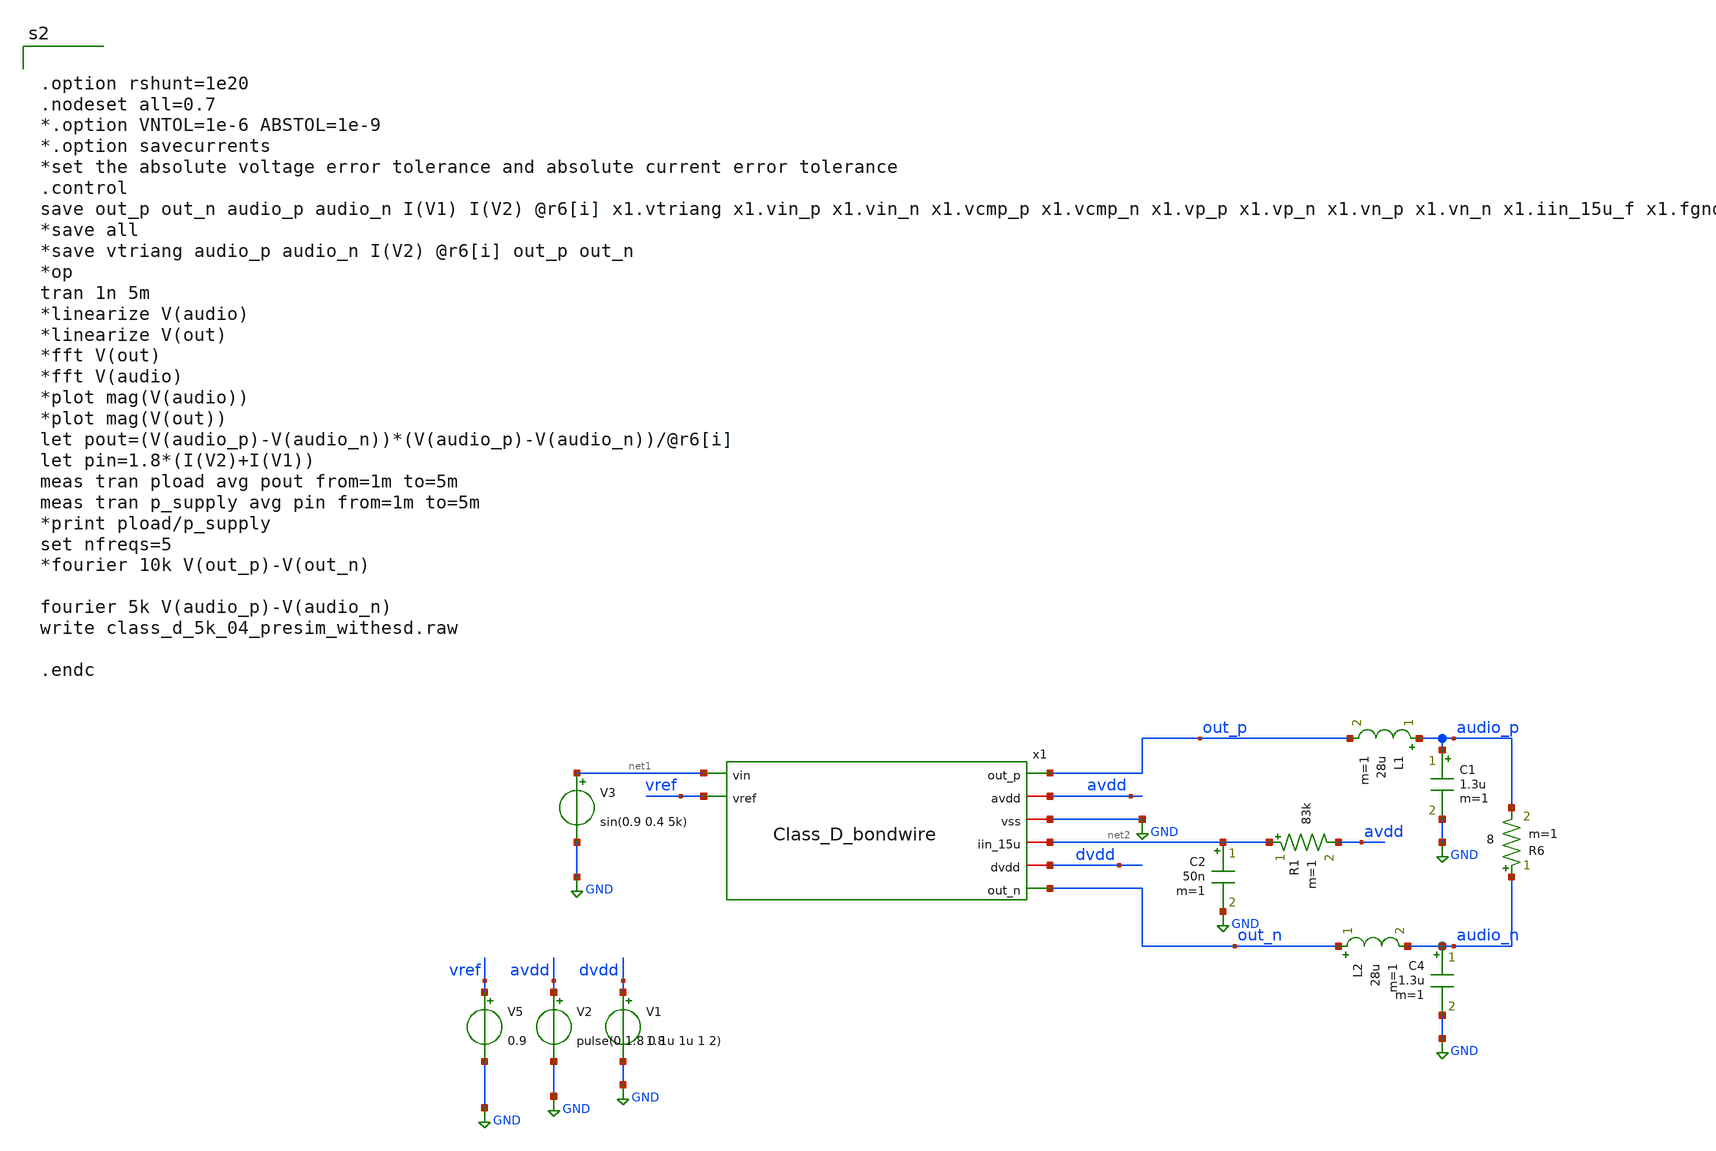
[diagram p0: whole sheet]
** sch_path: xschem/src/Class_D/Class_D_tb2.sch
**.subckt Class_D_tb2
V5 vref GND 0.9
V1 dvdd GND 1.8
V2 avdd GND pulse(0 1.8 0 1u 1u 1 2)
V3 net1 GND sin(0.9 0.4 5k)
L1 audio_p out_p 28u m=1
C1 audio_p GND 1.3u m=1
L2 out_n audio_n 28u m=1
C4 audio_n GND 1.3u m=1
R6 audio_n audio_p 8 m=1
x1 out_p net1 avdd vref GND net2 dvdd out_n Class_D_bondwire
R1 net2 avdd 83k m=1
C2 net2 GND 50n m=1
**** begin user architecture code

.include /home/eda/pdk/skywater-pdk/libraries/sky130_fd_pr_ngspice/latest/models/corners/tt.spice
.include /home/eda/magic/class_d_audio_amplifier/Class_D/Class_D_post.spice

* Resistor$::SKYWATER_MODELS/Capacitor
.include $::SKYWATER_MODELS/models/r+c/res_typical__cap_typical.spice
.include $::SKYWATER_MODELS/models/r+c/res_typical__cap_typical__lin.spice
* Special cells
.include $::SKYWATER_MODELS/models/corners/tt/specialized_cells.spice




.option rshunt=1e20
.nodeset all=0.7
*.option VNTOL=1e-6 ABSTOL=1e-9
*.option savecurrents
*set the absolute voltage error tolerance and absolute current error tolerance
.control
save out_p out_n audio_p audio_n I(V1) I(V2) @r6[i] x1.vtriang x1.vin_p x1.vin_n x1.vcmp_p x1.vcmp_n
+ x1.vp_p x1.vp_n x1.vn_p x1.vn_n x1.iin_15u_f x1.fgnd
*save all
*save vtriang audio_p audio_n I(V2) @r6[i] out_p out_n
*op
tran 1n 5m
*linearize V(audio)
*linearize V(out)
*fft V(out)
*fft V(audio)
*plot mag(V(audio))
*plot mag(V(out))
let pout=(V(audio_p)-V(audio_n))*(V(audio_p)-V(audio_n))/@r6[i]
let pin=1.8*(I(V2)+I(V1))
meas tran pload avg pout from=1m to=5m
meas tran p_supply avg pin from=1m to=5m
*print pload/p_supply
set nfreqs=5
*fourier 10k V(out_p)-V(out_n)

fourier 5k V(audio_p)-V(audio_n)
write class_d_5k_04_presim_withesd.raw

.endc




**** end user architecture code
**.ends

* expanding   symbol:  src/Class_D/Class_D_bondwire.sym # of pins=8
** sym_path: xschem/src/Class_D/Class_D_bondwire.sym
** sch_path: xschem/src/Class_D/Class_D_bondwire.sch
.subckt Class_D_bondwire out_p vin avdd vref vss iin_15u dvdd out_n
*.opin out_p
*.opin out_n
*.ipin vin
*.ipin vref
*.iopin avdd
*.iopin vss
*.iopin iin_15u
*.iopin dvdd
x1 vp_p out_p_f vp_n vin_p vcmp_p vtriang vin_f avdd_f vin_n fgnd vcmp_n iin_15u_f vn_p dvdd_f vn_n
+ out_n_f net8 Class_D
R1 net1 out_p_f 0.2m m=1
L1 out_p net1 0.011n m=1
C1 out_p vss 0.06p m=1
C2 out_p_f vss 0.06p m=1
R2 net2 avdd_f 0.3m m=1
L2 avdd net2 0.016n m=1
C3 avdd vss 0.04p m=1
C4 avdd_f vss 0.04p m=1
R3 net3 iin_15u_f 0.6m m=1
L3 iin_15u net3 0.032n m=1
C5 iin_15u vss 0.02p m=1
C6 iin_15u_f vss 0.02p m=1
R4 net4 dvdd_f 0.2m m=1
L4 dvdd net4 0.011n m=1
C7 dvdd vss 0.06p m=1
C8 dvdd_f vss 0.06p m=1
R5 net5 out_n_f 0.2m m=1
L5 out_n net5 0.011n m=1
C9 out_n vss 0.06p m=1
C10 out_n_f vss 0.06p m=1
R6 net6 vin_f 0.6m m=1
L6 vin net6 0.032n m=1
C11 vin vss 0.02p m=1
C12 vin_f vss 0.02p m=1
R7 net7 net8 0.6m m=1
L7 vref net7 0.032n m=1
C13 vref vss 0.02p m=1
C14 net8 vss 0.02p m=1
R8 net9 fgnd 0.15m m=1
L8 vss net9 0.008n m=1
C15 vss vss 0.08p m=1
C16 fgnd vss 0.08p m=1
x2 dvdd_f out_p_f fgnd ESD
x3 avdd_f iin_15u_f fgnd ESD
x4 dvdd_f out_n_f fgnd ESD
x5 avdd_f vin_f fgnd ESD
x6 avdd_f net8 fgnd ESD
x7 avdd_f fgnd io_clamp
x8 dvdd_f fgnd io_clamp
.ends


* expanding   symbol:  src/Class_D/Class_D.sym # of pins=17
** sym_path: xschem/src/Class_D/Class_D.sym
** sch_path: xschem/src/Class_D/Class_D.sch
.subckt Class_D vp_p out_p vp_n vin_p vcmp_p vtriang vin avdd vin_n vss vcmp_n iin_15u vn_p dvdd
+ vn_n out_n vref
*.ipin vin
*.iopin avdd
*.opin out_n
*.iopin vss
*.iopin iin_15u
*.opin out_p
*.opin vtriang
*.iopin dvdd
*.opin vin_p
*.opin vin_n
*.opin vcmp_p
*.opin vcmp_n
*.opin vp_p
*.opin vp_n
*.opin vn_p
*.opin vn_n
*.ipin vref
x1 avdd vbias3 vbias6 vin vref vss vin_n vin_p S_to_D
x2 avdd vbias5 vbias4 vref vss vsquare vtriang triangle
x3 avdd feedback_p vbias2 vref vss error_p integrator
x4 avdd feedback_n vbias7 vref vss error_n integrator
x5 avdd error_p vtriang vbias1 vss vcmp_p comparator
x6 avdd error_n vtriang vbias8 vss vcmp_n comparator
x7 dvdd vcmp_p vp_p vp_n vss dead_time
x8 dvdd vcmp_n vn_p vn_n vss dead_time
x10 iin_15u vbias1 vbias2 vbias3 vbias4 vbias5 vbias6 vbias7 vbias8 vss biasing_network
XR1 feedback_p vin_p vss sky130_fd_pr__res_xhigh_po W=0.35 L=35 mult=1 m=1
XR2 vin_n feedback_n vss sky130_fd_pr__res_xhigh_po W=0.35 L=35 mult=1 m=1
x9 dvdd vp_p out_p vss vp_n dvdd vn_p out_n vn_n output_driver
XC1 vss dvdd sky130_fd_pr__cap_mim_m3_2 W=16 L=16 MF=90 m=90
XC2 dvdd vss sky130_fd_pr__cap_mim_m3_2 W=30 L=30 MF=262 m=262
XC3 avdd vss sky130_fd_pr__cap_mim_m3_2 W=30 L=30 MF=132 m=132
XC4 avdd vss sky130_fd_pr__cap_mim_m3_2 W=30 L=30 MF=132 m=132
XR3 out_p feedback_p vss sky130_fd_pr__res_xhigh_po W=0.35 L=35 mult=1 m=1
XR4 out_n feedback_n vss sky130_fd_pr__res_xhigh_po W=0.35 L=35 mult=1 m=1
XC5 iin_15u vss sky130_fd_pr__cap_mim_m3_2 W=30 L=30 MF=210 m=210
.ends


* expanding   symbol:  src/ESD/ESD.sym # of pins=3
** sym_path: xschem/src/ESD/ESD.sym
** sch_path: xschem/src/ESD/ESD.sch
.subckt ESD vdd vin vss
*.iopin vdd
*.iopin vin
*.iopin vss
XD17 vin vdd sky130_fd_pr__diode_pd2nw_05v5 area=22500 pj=4e6
XD1 vss vin sky130_fd_pr__diode_pw2nd_05v5 area=22500 pj=4e6
.ends


* expanding   symbol:  src/ESD/io_clamp.sym # of pins=2
** sym_path: xschem/src/ESD/io_clamp.sym
** sch_path: xschem/src/ESD/io_clamp.sch
.subckt io_clamp vdd vss
*.iopin vdd
*.iopin vss
XD4 net3 net2 sky130_fd_pr__diode_pd2nw_05v5 area=22500 pj=4e6
XD1 net1 net3 sky130_fd_pr__diode_pd2nw_05v5 area=22500 pj=4e6
XD2 vdd net1 sky130_fd_pr__diode_pd2nw_05v5 area=22500 pj=4e6
XD3 net2 vss sky130_fd_pr__diode_pd2nw_05v5 area=22500 pj=4e6
.ends


* expanding   symbol:  src/S_to_D/S_to_D.sym # of pins=8
** sym_path: xschem/src/S_to_D/S_to_D.sym
** sch_path: xschem/src/S_to_D/S_to_D.sch
.subckt S_to_D vdd vbias1 vbias2 vi vref vss vn vp
*.iopin vdd
*.iopin vss
*.ipin vi
*.opin vp
*.opin vn
*.ipin vref
*.ipin vbias1
*.ipin vbias2
x1 vdd vref v1 vbias2 vss vn OTA
XR2 vn v1 vss sky130_fd_pr__res_xhigh_po L=10 mult=1 m=1
x2 vdd vi vp vbias1 vss vp OTA
XR1 v1 vi vss sky130_fd_pr__res_xhigh_po L=10 mult=1 m=1
.ends


* expanding   symbol:  src/triangle/triangle.sym # of pins=7
** sym_path: xschem/src/triangle/triangle.sym
** sch_path: xschem/src/triangle/triangle.sch
.subckt triangle vdd vbias1 vbias2 vref vss vsquare vt
*.iopin vdd
*.ipin vbias1
*.opin vt
*.ipin vref
*.opin vsquare
*.iopin vss
*.ipin vbias2
XR3 vsquare vi vss sky130_fd_pr__res_xhigh_po L=32 mult=1 m=1
XR1 vt vcmp vss sky130_fd_pr__res_xhigh_po L=4 mult=1 m=1
XR2 vcmp vsquare vss sky130_fd_pr__res_xhigh_po L=9 mult=1 m=1
x1 vdd vref vi vbias1 vss vt OTA_tri
x2 vdd vcmp vref vbias2 vss vsquare OTA
XC1 vi vt sky130_fd_pr__cap_mim_m3_1 W=15 L=15 MF=8 m=8
.ends


* expanding   symbol:  src/integrator/integrator.sym # of pins=6
** sym_path: xschem/src/integrator/integrator.sym
** sch_path: xschem/src/integrator/integrator.sch
.subckt integrator vdd vi vbias vref vss vout
*.ipin vi
*.ipin vbias
*.iopin vss
*.iopin vdd
*.opin vout
*.ipin vref
x1 vdd vref vi vbias vss vout OTA_int
XC1 vi vout sky130_fd_pr__cap_mim_m3_1 W=17.5 L=17.5 MF=16 m=16
.ends


* expanding   symbol:  src/comparator/comparator.sym # of pins=6
** sym_path: xschem/src/comparator/comparator.sym
** sch_path: xschem/src/comparator/comparator.sch
.subckt comparator vdd vp vn vbias vss vout
*.ipin vp
*.ipin vn
*.ipin vbias
*.iopin vss
*.iopin vdd
*.opin vout
XM1 v1 vp vc vc sky130_fd_pr__pfet_01v8_lvt L=1 W=4 nf=1 ad='int((nf+1)/2) * W/nf * 0.29' as='int((nf+2)/2) * W/nf * 0.29'
+ pd='2*int((nf+1)/2) * (W/nf + 0.29)' ps='2*int((nf+2)/2) * (W/nf + 0.29)' nrd='0.29 / W' nrs='0.29 / W'
+ sa=0 sb=0 sd=0 mult=16 m=16
XM2 vf vn vc vc sky130_fd_pr__pfet_01v8_lvt L=1 W=4 nf=1 ad='int((nf+1)/2) * W/nf * 0.29' as='int((nf+2)/2) * W/nf * 0.29'
+ pd='2*int((nf+1)/2) * (W/nf + 0.29)' ps='2*int((nf+2)/2) * (W/nf + 0.29)' nrd='0.29 / W' nrs='0.29 / W'
+ sa=0 sb=0 sd=0 mult=16 m=16
XM3 vc vbias vdd vdd sky130_fd_pr__pfet_01v8_lvt L=1 W=2 nf=2 ad='int((nf+1)/2) * W/nf * 0.29' as='int((nf+2)/2) * W/nf * 0.29'
+ pd='2*int((nf+1)/2) * (W/nf + 0.29)' ps='2*int((nf+2)/2) * (W/nf + 0.29)' nrd='0.29 / W' nrs='0.29 / W'
+ sa=0 sb=0 sd=0 mult=24 m=24
XM4 v1 vf vss vss sky130_fd_pr__nfet_01v8_lvt L=1 W=1 nf=1 ad='int((nf+1)/2) * W/nf * 0.29' as='int((nf+2)/2) * W/nf * 0.29'
+ pd='2*int((nf+1)/2) * (W/nf + 0.29)' ps='2*int((nf+2)/2) * (W/nf + 0.29)' nrd='0.29 / W' nrs='0.29 / W'
+ sa=0 sb=0 sd=0 mult=16 m=16
XM5 vf vf vss vss sky130_fd_pr__nfet_01v8_lvt L=1 W=1 nf=1 ad='int((nf+1)/2) * W/nf * 0.29' as='int((nf+2)/2) * W/nf * 0.29'
+ pd='2*int((nf+1)/2) * (W/nf + 0.29)' ps='2*int((nf+2)/2) * (W/nf + 0.29)' nrd='0.29 / W' nrs='0.29 / W'
+ sa=0 sb=0 sd=0 mult=16 m=16
XM6 vbias vbias vdd vdd sky130_fd_pr__pfet_01v8_lvt L=1 W=2 nf=2 ad='int((nf+1)/2) * W/nf * 0.29' as='int((nf+2)/2) * W/nf * 0.29'
+ pd='2*int((nf+1)/2) * (W/nf + 0.29)' ps='2*int((nf+2)/2) * (W/nf + 0.29)' nrd='0.29 / W' nrs='0.29 / W'
+ sa=0 sb=0 sd=0 mult=24 m=24
XM7 vout vbias vdd vdd sky130_fd_pr__pfet_01v8_lvt L=1 W=2 nf=2 ad='int((nf+1)/2) * W/nf * 0.29' as='int((nf+2)/2) * W/nf * 0.29'
+ pd='2*int((nf+1)/2) * (W/nf + 0.29)' ps='2*int((nf+2)/2) * (W/nf + 0.29)' nrd='0.29 / W' nrs='0.29 / W'
+ sa=0 sb=0 sd=0 mult=48 m=48
XM8 vout v1 vss vss sky130_fd_pr__nfet_01v8_lvt L=1 W=1 nf=1 ad='int((nf+1)/2) * W/nf * 0.29' as='int((nf+2)/2) * W/nf * 0.29'
+ pd='2*int((nf+1)/2) * (W/nf + 0.29)' ps='2*int((nf+2)/2) * (W/nf + 0.29)' nrd='0.29 / W' nrs='0.29 / W'
+ sa=0 sb=0 sd=0 mult=64 m=64
.ends


* expanding   symbol:  src/dead_time/dead_time.sym # of pins=5
** sym_path: xschem/src/dead_time/dead_time.sym
** sch_path: xschem/src/dead_time/dead_time.sch
.subckt dead_time vdd vin vp vn vss
*.ipin vin
*.iopin vdd
*.opin vp
*.iopin vss
*.opin vn
x1 vdd vin vinn vss inverter
x2 vdd net1 vin net4 vss nand
x3 vdd net2 net3 vinn vss nand
XC1 net1 vss sky130_fd_pr__cap_mim_m3_1 W=17.75 L=17.75 MF=16 m=16
XM3 net5 net1 vss vss sky130_fd_pr__nfet_01v8 L=0.15 W=5 nf=2 ad='int((nf+1)/2) * W/nf * 0.29' as='int((nf+2)/2) * W/nf * 0.29'
+ pd='2*int((nf+1)/2) * (W/nf + 0.29)' ps='2*int((nf+2)/2) * (W/nf + 0.29)' nrd='0.29 / W' nrs='0.29 / W'
+ sa=0 sb=0 sd=0 mult=1 m=1
XM1 net5 net1 vdd vdd sky130_fd_pr__pfet_01v8 L=0.15 W=10 nf=2 ad='int((nf+1)/2) * W/nf * 0.29' as='int((nf+2)/2) * W/nf * 0.29'
+ pd='2*int((nf+1)/2) * (W/nf + 0.29)' ps='2*int((nf+2)/2) * (W/nf + 0.29)' nrd='0.29 / W' nrs='0.29 / W'
+ sa=0 sb=0 sd=0 mult=1 m=1
XM2 net3 net5 vss vss sky130_fd_pr__nfet_01v8 L=0.15 W=20 nf=8 ad='int((nf+1)/2) * W/nf * 0.29' as='int((nf+2)/2) * W/nf * 0.29'
+ pd='2*int((nf+1)/2) * (W/nf + 0.29)' ps='2*int((nf+2)/2) * (W/nf + 0.29)' nrd='0.29 / W' nrs='0.29 / W'
+ sa=0 sb=0 sd=0 mult=1 m=1
XM4 net3 net5 vdd vdd sky130_fd_pr__pfet_01v8 L=0.15 W=40 nf=8 ad='int((nf+1)/2) * W/nf * 0.29' as='int((nf+2)/2) * W/nf * 0.29'
+ pd='2*int((nf+1)/2) * (W/nf + 0.29)' ps='2*int((nf+2)/2) * (W/nf + 0.29)' nrd='0.29 / W' nrs='0.29 / W'
+ sa=0 sb=0 sd=0 mult=1 m=1
XM5 net6 net3 vss vss sky130_fd_pr__nfet_01v8 L=0.15 W=90 nf=36 ad='int((nf+1)/2) * W/nf * 0.29' as='int((nf+2)/2) * W/nf * 0.29'
+ pd='2*int((nf+1)/2) * (W/nf + 0.29)' ps='2*int((nf+2)/2) * (W/nf + 0.29)' nrd='0.29 / W' nrs='0.29 / W'
+ sa=0 sb=0 sd=0 mult=1 m=1
XM6 net6 net3 vdd vdd sky130_fd_pr__pfet_01v8 L=0.15 W=180 nf=36 ad='int((nf+1)/2) * W/nf * 0.29' as='int((nf+2)/2) * W/nf * 0.29'
+ pd='2*int((nf+1)/2) * (W/nf + 0.29)' ps='2*int((nf+2)/2) * (W/nf + 0.29)' nrd='0.29 / W' nrs='0.29 / W'
+ sa=0 sb=0 sd=0 mult=1 m=1
XM7 vp net6 vss vss sky130_fd_pr__nfet_01v8 L=0.15 W=200 nf=81 ad='int((nf+1)/2) * W/nf * 0.29' as='int((nf+2)/2) * W/nf * 0.29'
+ pd='2*int((nf+1)/2) * (W/nf + 0.29)' ps='2*int((nf+2)/2) * (W/nf + 0.29)' nrd='0.29 / W' nrs='0.29 / W'
+ sa=0 sb=0 sd=0 mult=2 m=2
XM8 vp net6 vdd vdd sky130_fd_pr__pfet_01v8 L=0.15 W=400 nf=81 ad='int((nf+1)/2) * W/nf * 0.29' as='int((nf+2)/2) * W/nf * 0.29'
+ pd='2*int((nf+1)/2) * (W/nf + 0.29)' ps='2*int((nf+2)/2) * (W/nf + 0.29)' nrd='0.29 / W' nrs='0.29 / W'
+ sa=0 sb=0 sd=0 mult=2 m=2
XM9 net7 net2 vss vss sky130_fd_pr__nfet_01v8 L=0.15 W=5 nf=2 ad='int((nf+1)/2) * W/nf * 0.29' as='int((nf+2)/2) * W/nf * 0.29'
+ pd='2*int((nf+1)/2) * (W/nf + 0.29)' ps='2*int((nf+2)/2) * (W/nf + 0.29)' nrd='0.29 / W' nrs='0.29 / W'
+ sa=0 sb=0 sd=0 mult=1 m=1
XM10 net7 net2 vdd vdd sky130_fd_pr__pfet_01v8 L=0.15 W=10 nf=2 ad='int((nf+1)/2) * W/nf * 0.29' as='int((nf+2)/2) * W/nf * 0.29'
+ pd='2*int((nf+1)/2) * (W/nf + 0.29)' ps='2*int((nf+2)/2) * (W/nf + 0.29)' nrd='0.29 / W' nrs='0.29 / W'
+ sa=0 sb=0 sd=0 mult=1 m=1
XM11 net4 net7 vss vss sky130_fd_pr__nfet_01v8 L=0.15 W=20 nf=8 ad='int((nf+1)/2) * W/nf * 0.29' as='int((nf+2)/2) * W/nf * 0.29'
+ pd='2*int((nf+1)/2) * (W/nf + 0.29)' ps='2*int((nf+2)/2) * (W/nf + 0.29)' nrd='0.29 / W' nrs='0.29 / W'
+ sa=0 sb=0 sd=0 mult=1 m=1
XM12 net4 net7 vdd vdd sky130_fd_pr__pfet_01v8 L=0.15 W=40 nf=8 ad='int((nf+1)/2) * W/nf * 0.29' as='int((nf+2)/2) * W/nf * 0.29'
+ pd='2*int((nf+1)/2) * (W/nf + 0.29)' ps='2*int((nf+2)/2) * (W/nf + 0.29)' nrd='0.29 / W' nrs='0.29 / W'
+ sa=0 sb=0 sd=0 mult=1 m=1
XM13 vn net4 vss vss sky130_fd_pr__nfet_01v8 L=0.15 W=90 nf=36 ad='int((nf+1)/2) * W/nf * 0.29' as='int((nf+2)/2) * W/nf * 0.29'
+ pd='2*int((nf+1)/2) * (W/nf + 0.29)' ps='2*int((nf+2)/2) * (W/nf + 0.29)' nrd='0.29 / W' nrs='0.29 / W'
+ sa=0 sb=0 sd=0 mult=1 m=1
XM14 vn net4 vdd vdd sky130_fd_pr__pfet_01v8 L=0.15 W=180 nf=36 ad='int((nf+1)/2) * W/nf * 0.29' as='int((nf+2)/2) * W/nf * 0.29'
+ pd='2*int((nf+1)/2) * (W/nf + 0.29)' ps='2*int((nf+2)/2) * (W/nf + 0.29)' nrd='0.29 / W' nrs='0.29 / W'
+ sa=0 sb=0 sd=0 mult=1 m=1
XC2 net2 vss sky130_fd_pr__cap_mim_m3_1 W=17.75 L=17.75 MF=16 m=16
.ends


* expanding   symbol:  src/biasing_network/biasing_network.sym # of pins=10
** sym_path: xschem/src/biasing_network/biasing_network.sym
** sch_path: xschem/src/biasing_network/biasing_network.sch
.subckt biasing_network iin_15u ibias1_15u ibias2_15u ibias3_15u ibias4_15u ibias5_15u ibias6_15u
+ ibias7_15u ibias8_15u vss
*.iopin iin_15u
*.iopin vss
*.opin ibias1_15u
*.opin ibias2_15u
*.opin ibias3_15u
*.opin ibias4_15u
*.opin ibias5_15u
*.opin ibias6_15u
*.opin ibias7_15u
*.opin ibias8_15u
XM5 iin_15u iin_15u vss vss sky130_fd_pr__nfet_01v8_lvt L=2 W=4 nf=2 ad='int((nf+1)/2) * W/nf * 0.29'
+ as='int((nf+2)/2) * W/nf * 0.29' pd='2*int((nf+1)/2) * (W/nf + 0.29)' ps='2*int((nf+2)/2) * (W/nf + 0.29)'
+ nrd='0.29 / W' nrs='0.29 / W' sa=0 sb=0 sd=0 mult=8 m=8
XM6 ibias1_15u iin_15u vss vss sky130_fd_pr__nfet_01v8_lvt L=2 W=4 nf=2 ad='int((nf+1)/2) * W/nf * 0.29'
+ as='int((nf+2)/2) * W/nf * 0.29' pd='2*int((nf+1)/2) * (W/nf + 0.29)' ps='2*int((nf+2)/2) * (W/nf + 0.29)'
+ nrd='0.29 / W' nrs='0.29 / W' sa=0 sb=0 sd=0 mult=8 m=8
XM7 ibias2_15u iin_15u vss vss sky130_fd_pr__nfet_01v8_lvt L=2 W=4 nf=2 ad='int((nf+1)/2) * W/nf * 0.29'
+ as='int((nf+2)/2) * W/nf * 0.29' pd='2*int((nf+1)/2) * (W/nf + 0.29)' ps='2*int((nf+2)/2) * (W/nf + 0.29)'
+ nrd='0.29 / W' nrs='0.29 / W' sa=0 sb=0 sd=0 mult=8 m=8
XM8 ibias3_15u iin_15u vss vss sky130_fd_pr__nfet_01v8_lvt L=2 W=4 nf=2 ad='int((nf+1)/2) * W/nf * 0.29'
+ as='int((nf+2)/2) * W/nf * 0.29' pd='2*int((nf+1)/2) * (W/nf + 0.29)' ps='2*int((nf+2)/2) * (W/nf + 0.29)'
+ nrd='0.29 / W' nrs='0.29 / W' sa=0 sb=0 sd=0 mult=8 m=8
XM9 ibias4_15u iin_15u vss vss sky130_fd_pr__nfet_01v8_lvt L=2 W=4 nf=2 ad='int((nf+1)/2) * W/nf * 0.29'
+ as='int((nf+2)/2) * W/nf * 0.29' pd='2*int((nf+1)/2) * (W/nf + 0.29)' ps='2*int((nf+2)/2) * (W/nf + 0.29)'
+ nrd='0.29 / W' nrs='0.29 / W' sa=0 sb=0 sd=0 mult=8 m=8
XM10 ibias5_15u iin_15u vss vss sky130_fd_pr__nfet_01v8_lvt L=2 W=4 nf=2 ad='int((nf+1)/2) * W/nf * 0.29'
+ as='int((nf+2)/2) * W/nf * 0.29' pd='2*int((nf+1)/2) * (W/nf + 0.29)' ps='2*int((nf+2)/2) * (W/nf + 0.29)'
+ nrd='0.29 / W' nrs='0.29 / W' sa=0 sb=0 sd=0 mult=8 m=8
XM11 ibias6_15u iin_15u vss vss sky130_fd_pr__nfet_01v8_lvt L=2 W=4 nf=2 ad='int((nf+1)/2) * W/nf * 0.29'
+ as='int((nf+2)/2) * W/nf * 0.29' pd='2*int((nf+1)/2) * (W/nf + 0.29)' ps='2*int((nf+2)/2) * (W/nf + 0.29)'
+ nrd='0.29 / W' nrs='0.29 / W' sa=0 sb=0 sd=0 mult=8 m=8
XM12 vss iin_15u ibias7_15u vss sky130_fd_pr__nfet_01v8_lvt L=2 W=4 nf=2 ad='int((nf+1)/2) * W/nf * 0.29'
+ as='int((nf+2)/2) * W/nf * 0.29' pd='2*int((nf+1)/2) * (W/nf + 0.29)' ps='2*int((nf+2)/2) * (W/nf + 0.29)'
+ nrd='0.29 / W' nrs='0.29 / W' sa=0 sb=0 sd=0 mult=8 m=8
XM13 ibias8_15u iin_15u vss vss sky130_fd_pr__nfet_01v8_lvt L=2 W=4 nf=2 ad='int((nf+1)/2) * W/nf * 0.29'
+ as='int((nf+2)/2) * W/nf * 0.29' pd='2*int((nf+1)/2) * (W/nf + 0.29)' ps='2*int((nf+2)/2) * (W/nf + 0.29)'
+ nrd='0.29 / W' nrs='0.29 / W' sa=0 sb=0 sd=0 mult=8 m=8
.ends


* expanding   symbol:  src/output_driver/output_driver.sym # of pins=9
** sym_path: xschem/src/output_driver/output_driver.sym
** sch_path: xschem/src/output_driver/output_driver.sch
.subckt output_driver dvdd1 vp_p out_p vss vp_n dvdd2 vn_p out_n vn_n
*.ipin vp_p
*.ipin vp_n
*.ipin vn_p
*.ipin vn_n
*.opin out_p
*.opin out_n
*.iopin dvdd1
*.iopin vss
*.iopin dvdd2
x1 dvdd1 vss vp_p out_p vp_n half_driver
x2 dvdd2 vss vn_p out_n vn_n half_driver
.ends


* expanding   symbol:  src/OTA/OTA.sym # of pins=6
** sym_path: xschem/src/OTA/OTA.sym
** sch_path: xschem/src/OTA/OTA.sch
.subckt OTA vdd vp vn vbias vss vout
*.ipin vp
*.ipin vn
*.ipin vbias
*.iopin vss
*.iopin vdd
*.opin vout
XM1 v1 vp vc vc sky130_fd_pr__pfet_01v8_lvt L=1 W=4 nf=1 ad='int((nf+1)/2) * W/nf * 0.29' as='int((nf+2)/2) * W/nf * 0.29'
+ pd='2*int((nf+1)/2) * (W/nf + 0.29)' ps='2*int((nf+2)/2) * (W/nf + 0.29)' nrd='0.29 / W' nrs='0.29 / W'
+ sa=0 sb=0 sd=0 mult=16 m=16
XM2 vf vn vc vc sky130_fd_pr__pfet_01v8_lvt L=1 W=4 nf=1 ad='int((nf+1)/2) * W/nf * 0.29' as='int((nf+2)/2) * W/nf * 0.29'
+ pd='2*int((nf+1)/2) * (W/nf + 0.29)' ps='2*int((nf+2)/2) * (W/nf + 0.29)' nrd='0.29 / W' nrs='0.29 / W'
+ sa=0 sb=0 sd=0 mult=16 m=16
XM3 vc vbias vdd vdd sky130_fd_pr__pfet_01v8_lvt L=1 W=2 nf=2 ad='int((nf+1)/2) * W/nf * 0.29' as='int((nf+2)/2) * W/nf * 0.29'
+ pd='2*int((nf+1)/2) * (W/nf + 0.29)' ps='2*int((nf+2)/2) * (W/nf + 0.29)' nrd='0.29 / W' nrs='0.29 / W'
+ sa=0 sb=0 sd=0 mult=24 m=24
XM4 v1 vf vss vss sky130_fd_pr__nfet_01v8_lvt L=1 W=1 nf=1 ad='int((nf+1)/2) * W/nf * 0.29' as='int((nf+2)/2) * W/nf * 0.29'
+ pd='2*int((nf+1)/2) * (W/nf + 0.29)' ps='2*int((nf+2)/2) * (W/nf + 0.29)' nrd='0.29 / W' nrs='0.29 / W'
+ sa=0 sb=0 sd=0 mult=16 m=16
XM5 vf vf vss vss sky130_fd_pr__nfet_01v8_lvt L=1 W=1 nf=1 ad='int((nf+1)/2) * W/nf * 0.29' as='int((nf+2)/2) * W/nf * 0.29'
+ pd='2*int((nf+1)/2) * (W/nf + 0.29)' ps='2*int((nf+2)/2) * (W/nf + 0.29)' nrd='0.29 / W' nrs='0.29 / W'
+ sa=0 sb=0 sd=0 mult=16 m=16
XM6 vbias vbias vdd vdd sky130_fd_pr__pfet_01v8_lvt L=1 W=2 nf=2 ad='int((nf+1)/2) * W/nf * 0.29' as='int((nf+2)/2) * W/nf * 0.29'
+ pd='2*int((nf+1)/2) * (W/nf + 0.29)' ps='2*int((nf+2)/2) * (W/nf + 0.29)' nrd='0.29 / W' nrs='0.29 / W'
+ sa=0 sb=0 sd=0 mult=24 m=24
XM7 vout vbias vdd vdd sky130_fd_pr__pfet_01v8_lvt L=1 W=2 nf=2 ad='int((nf+1)/2) * W/nf * 0.29' as='int((nf+2)/2) * W/nf * 0.29'
+ pd='2*int((nf+1)/2) * (W/nf + 0.29)' ps='2*int((nf+2)/2) * (W/nf + 0.29)' nrd='0.29 / W' nrs='0.29 / W'
+ sa=0 sb=0 sd=0 mult=48 m=48
XM8 vout v1 vss vss sky130_fd_pr__nfet_01v8_lvt L=1 W=1 nf=1 ad='int((nf+1)/2) * W/nf * 0.29' as='int((nf+2)/2) * W/nf * 0.29'
+ pd='2*int((nf+1)/2) * (W/nf + 0.29)' ps='2*int((nf+2)/2) * (W/nf + 0.29)' nrd='0.29 / W' nrs='0.29 / W'
+ sa=0 sb=0 sd=0 mult=64 m=64
XR1 v1 net1 vss sky130_fd_pr__res_xhigh_po W=0.35 L=0.5 mult=1 m=1
XC2 net1 vout sky130_fd_pr__cap_mim_m3_1 W=14 L=14 MF=1 m=1
.ends


* expanding   symbol:  src/OTA_tri/OTA_tri.sym # of pins=6
** sym_path: xschem/src/OTA_tri/OTA_tri.sym
** sch_path: xschem/src/OTA_tri/OTA_tri.sch
.subckt OTA_tri vdd vp vn vbias vss vout
*.ipin vp
*.ipin vn
*.ipin vbias
*.iopin vss
*.iopin vdd
*.opin vout
XM1 v1 vp vc vc sky130_fd_pr__pfet_01v8_lvt L=1 W=4 nf=1 ad='int((nf+1)/2) * W/nf * 0.29' as='int((nf+2)/2) * W/nf * 0.29'
+ pd='2*int((nf+1)/2) * (W/nf + 0.29)' ps='2*int((nf+2)/2) * (W/nf + 0.29)' nrd='0.29 / W' nrs='0.29 / W'
+ sa=0 sb=0 sd=0 mult=16 m=16
XM2 vf vn vc vc sky130_fd_pr__pfet_01v8_lvt L=1 W=4 nf=1 ad='int((nf+1)/2) * W/nf * 0.29' as='int((nf+2)/2) * W/nf * 0.29'
+ pd='2*int((nf+1)/2) * (W/nf + 0.29)' ps='2*int((nf+2)/2) * (W/nf + 0.29)' nrd='0.29 / W' nrs='0.29 / W'
+ sa=0 sb=0 sd=0 mult=16 m=16
XM3 vc vbias vdd vdd sky130_fd_pr__pfet_01v8_lvt L=1 W=2 nf=2 ad='int((nf+1)/2) * W/nf * 0.29' as='int((nf+2)/2) * W/nf * 0.29'
+ pd='2*int((nf+1)/2) * (W/nf + 0.29)' ps='2*int((nf+2)/2) * (W/nf + 0.29)' nrd='0.29 / W' nrs='0.29 / W'
+ sa=0 sb=0 sd=0 mult=24 m=24
XM4 v1 vf vss vss sky130_fd_pr__nfet_01v8_lvt L=1 W=1 nf=1 ad='int((nf+1)/2) * W/nf * 0.29' as='int((nf+2)/2) * W/nf * 0.29'
+ pd='2*int((nf+1)/2) * (W/nf + 0.29)' ps='2*int((nf+2)/2) * (W/nf + 0.29)' nrd='0.29 / W' nrs='0.29 / W'
+ sa=0 sb=0 sd=0 mult=16 m=16
XM5 vf vf vss vss sky130_fd_pr__nfet_01v8_lvt L=1 W=1 nf=1 ad='int((nf+1)/2) * W/nf * 0.29' as='int((nf+2)/2) * W/nf * 0.29'
+ pd='2*int((nf+1)/2) * (W/nf + 0.29)' ps='2*int((nf+2)/2) * (W/nf + 0.29)' nrd='0.29 / W' nrs='0.29 / W'
+ sa=0 sb=0 sd=0 mult=16 m=16
XM6 vbias vbias vdd vdd sky130_fd_pr__pfet_01v8_lvt L=1 W=2 nf=2 ad='int((nf+1)/2) * W/nf * 0.29' as='int((nf+2)/2) * W/nf * 0.29'
+ pd='2*int((nf+1)/2) * (W/nf + 0.29)' ps='2*int((nf+2)/2) * (W/nf + 0.29)' nrd='0.29 / W' nrs='0.29 / W'
+ sa=0 sb=0 sd=0 mult=24 m=24
XM7 vout vbias vdd vdd sky130_fd_pr__pfet_01v8_lvt L=1 W=2 nf=3 ad='int((nf+1)/2) * W/nf * 0.29' as='int((nf+2)/2) * W/nf * 0.29'
+ pd='2*int((nf+1)/2) * (W/nf + 0.29)' ps='2*int((nf+2)/2) * (W/nf + 0.29)' nrd='0.29 / W' nrs='0.29 / W'
+ sa=0 sb=0 sd=0 mult=48 m=48
XM8 vout v1 vss vss sky130_fd_pr__nfet_01v8_lvt L=1 W=1 nf=1 ad='int((nf+1)/2) * W/nf * 0.29' as='int((nf+2)/2) * W/nf * 0.29'
+ pd='2*int((nf+1)/2) * (W/nf + 0.29)' ps='2*int((nf+2)/2) * (W/nf + 0.29)' nrd='0.29 / W' nrs='0.29 / W'
+ sa=0 sb=0 sd=0 mult=64 m=64
XC1 net1 vout sky130_fd_pr__cap_mim_m3_1 W=27 L=18 MF=1 m=1
XR1 v1 net1 vss sky130_fd_pr__res_xhigh_po W=0.35 L=1.4 mult=1 m=1
.ends


* expanding   symbol:  src/OTA_int/OTA_int.sym # of pins=6
** sym_path: xschem/src/OTA_int/OTA_int.sym
** sch_path: xschem/src/OTA_int/OTA_int.sch
.subckt OTA_int vdd vp vn vbias vss vout
*.ipin vp
*.ipin vn
*.ipin vbias
*.iopin vss
*.iopin vdd
*.opin vout
XM1 v1 vp vc vc sky130_fd_pr__pfet_01v8_lvt L=1 W=4 nf=1 ad='int((nf+1)/2) * W/nf * 0.29' as='int((nf+2)/2) * W/nf * 0.29'
+ pd='2*int((nf+1)/2) * (W/nf + 0.29)' ps='2*int((nf+2)/2) * (W/nf + 0.29)' nrd='0.29 / W' nrs='0.29 / W'
+ sa=0 sb=0 sd=0 mult=16 m=16
XM2 vf vn vc vc sky130_fd_pr__pfet_01v8_lvt L=1 W=4 nf=1 ad='int((nf+1)/2) * W/nf * 0.29' as='int((nf+2)/2) * W/nf * 0.29'
+ pd='2*int((nf+1)/2) * (W/nf + 0.29)' ps='2*int((nf+2)/2) * (W/nf + 0.29)' nrd='0.29 / W' nrs='0.29 / W'
+ sa=0 sb=0 sd=0 mult=16 m=16
XM3 vc vbias vdd vdd sky130_fd_pr__pfet_01v8_lvt L=1 W=2 nf=2 ad='int((nf+1)/2) * W/nf * 0.29' as='int((nf+2)/2) * W/nf * 0.29'
+ pd='2*int((nf+1)/2) * (W/nf + 0.29)' ps='2*int((nf+2)/2) * (W/nf + 0.29)' nrd='0.29 / W' nrs='0.29 / W'
+ sa=0 sb=0 sd=0 mult=24 m=24
XM4 v1 vf vss vss sky130_fd_pr__nfet_01v8_lvt L=1 W=1 nf=1 ad='int((nf+1)/2) * W/nf * 0.29' as='int((nf+2)/2) * W/nf * 0.29'
+ pd='2*int((nf+1)/2) * (W/nf + 0.29)' ps='2*int((nf+2)/2) * (W/nf + 0.29)' nrd='0.29 / W' nrs='0.29 / W'
+ sa=0 sb=0 sd=0 mult=16 m=16
XM5 vf vf vss vss sky130_fd_pr__nfet_01v8_lvt L=1 W=1 nf=1 ad='int((nf+1)/2) * W/nf * 0.29' as='int((nf+2)/2) * W/nf * 0.29'
+ pd='2*int((nf+1)/2) * (W/nf + 0.29)' ps='2*int((nf+2)/2) * (W/nf + 0.29)' nrd='0.29 / W' nrs='0.29 / W'
+ sa=0 sb=0 sd=0 mult=16 m=16
XM6 vbias vbias vdd vdd sky130_fd_pr__pfet_01v8_lvt L=1 W=2 nf=2 ad='int((nf+1)/2) * W/nf * 0.29' as='int((nf+2)/2) * W/nf * 0.29'
+ pd='2*int((nf+1)/2) * (W/nf + 0.29)' ps='2*int((nf+2)/2) * (W/nf + 0.29)' nrd='0.29 / W' nrs='0.29 / W'
+ sa=0 sb=0 sd=0 mult=24 m=24
XM7 vout vbias vdd vdd sky130_fd_pr__pfet_01v8_lvt L=1 W=2 nf=2 ad='int((nf+1)/2) * W/nf * 0.29' as='int((nf+2)/2) * W/nf * 0.29'
+ pd='2*int((nf+1)/2) * (W/nf + 0.29)' ps='2*int((nf+2)/2) * (W/nf + 0.29)' nrd='0.29 / W' nrs='0.29 / W'
+ sa=0 sb=0 sd=0 mult=48 m=48
XM8 vout v1 vss vss sky130_fd_pr__nfet_01v8_lvt L=1 W=1 nf=1 ad='int((nf+1)/2) * W/nf * 0.29' as='int((nf+2)/2) * W/nf * 0.29'
+ pd='2*int((nf+1)/2) * (W/nf + 0.29)' ps='2*int((nf+2)/2) * (W/nf + 0.29)' nrd='0.29 / W' nrs='0.29 / W'
+ sa=0 sb=0 sd=0 mult=64 m=64
XC1 v2 vout sky130_fd_pr__cap_mim_m3_1 W=14 L=30 MF=1 m=1
XR1 v1 v2 vss sky130_fd_pr__res_xhigh_po L=2.8 mult=1 m=1
XC2 v2 vout sky130_fd_pr__cap_mim_m3_1 W=30 L=14 MF=1 m=1
.ends


* expanding   symbol:  src/inverter/inverter.sym # of pins=4
** sym_path: xschem/src/inverter/inverter.sym
** sch_path: xschem/src/inverter/inverter.sch
.subckt inverter vdd A B vss
*.iopin vdd
*.iopin vss
*.ipin A
*.opin B
XM3 B A vss vss sky130_fd_pr__nfet_01v8 L=0.15 W=1 nf=1 ad='int((nf+1)/2) * W/nf * 0.29' as='int((nf+2)/2) * W/nf * 0.29'
+ pd='2*int((nf+1)/2) * (W/nf + 0.29)' ps='2*int((nf+2)/2) * (W/nf + 0.29)' nrd='0.29 / W' nrs='0.29 / W'
+ sa=0 sb=0 sd=0 mult=1 m=1
XM1 B A vdd vdd sky130_fd_pr__pfet_01v8 L=0.15 W=2 nf=1 ad='int((nf+1)/2) * W/nf * 0.29' as='int((nf+2)/2) * W/nf * 0.29'
+ pd='2*int((nf+1)/2) * (W/nf + 0.29)' ps='2*int((nf+2)/2) * (W/nf + 0.29)' nrd='0.29 / W' nrs='0.29 / W'
+ sa=0 sb=0 sd=0 mult=1 m=1
.ends


* expanding   symbol:  src/nand/nand.sym # of pins=5
** sym_path: xschem/src/nand/nand.sym
** sch_path: xschem/src/nand/nand.sch
.subckt nand vdd out A B vss
*.ipin A
*.ipin B
*.opin out
*.iopin vdd
*.iopin vss
XM1 out A net1 vss sky130_fd_pr__nfet_01v8 L=0.15 W=2 nf=1 ad='int((nf+1)/2) * W/nf * 0.29' as='int((nf+2)/2) * W/nf * 0.29'
+ pd='2*int((nf+1)/2) * (W/nf + 0.29)' ps='2*int((nf+2)/2) * (W/nf + 0.29)' nrd='0.29 / W' nrs='0.29 / W'
+ sa=0 sb=0 sd=0 mult=1 m=1
XM2 out A vdd vdd sky130_fd_pr__pfet_01v8 L=0.15 W=2 nf=1 ad='int((nf+1)/2) * W/nf * 0.29' as='int((nf+2)/2) * W/nf * 0.29'
+ pd='2*int((nf+1)/2) * (W/nf + 0.29)' ps='2*int((nf+2)/2) * (W/nf + 0.29)' nrd='0.29 / W' nrs='0.29 / W'
+ sa=0 sb=0 sd=0 mult=1 m=1
XM3 net1 B vss vss sky130_fd_pr__nfet_01v8 L=0.15 W=2 nf=1 ad='int((nf+1)/2) * W/nf * 0.29' as='int((nf+2)/2) * W/nf * 0.29'
+ pd='2*int((nf+1)/2) * (W/nf + 0.29)' ps='2*int((nf+2)/2) * (W/nf + 0.29)' nrd='0.29 / W' nrs='0.29 / W'
+ sa=0 sb=0 sd=0 mult=1 m=1
XM4 out B vdd vdd sky130_fd_pr__pfet_01v8 L=0.15 W=2 nf=1 ad='int((nf+1)/2) * W/nf * 0.29' as='int((nf+2)/2) * W/nf * 0.29'
+ pd='2*int((nf+1)/2) * (W/nf + 0.29)' ps='2*int((nf+2)/2) * (W/nf + 0.29)' nrd='0.29 / W' nrs='0.29 / W'
+ sa=0 sb=0 sd=0 mult=1 m=1
.ends


* expanding   symbol:  src/output_driver/half_driver.sym # of pins=5
** sym_path: xschem/src/output_driver/half_driver.sym
** sch_path: xschem/src/output_driver/half_driver.sch
.subckt half_driver vdd vss vp_p out_p vp_n
*.ipin vp_p
*.ipin vp_n
*.opin out_p
*.iopin vdd
*.iopin vss
XM1 out_p vp_p vdd vdd sky130_fd_pr__pfet_01v8 L=0.15 W=12000 nf=200 ad='int((nf+1)/2) * W/nf * 0.29'
+ as='int((nf+2)/2) * W/nf * 0.29' pd='2*int((nf+1)/2) * (W/nf + 0.29)' ps='2*int((nf+2)/2) * (W/nf + 0.29)'
+ nrd='0.29 / W' nrs='0.29 / W' sa=0 sb=0 sd=0 mult=1 m=1
XM2 out_p vp_n vss vss sky130_fd_pr__nfet_01v8 L=0.15 W=2400 nf=100 ad='int((nf+1)/2) * W/nf * 0.29'
+ as='int((nf+2)/2) * W/nf * 0.29' pd='2*int((nf+1)/2) * (W/nf + 0.29)' ps='2*int((nf+2)/2) * (W/nf + 0.29)'
+ nrd='0.29 / W' nrs='0.29 / W' sa=0 sb=0 sd=0 mult=1 m=1
.ends

.GLOBAL GND
.end
